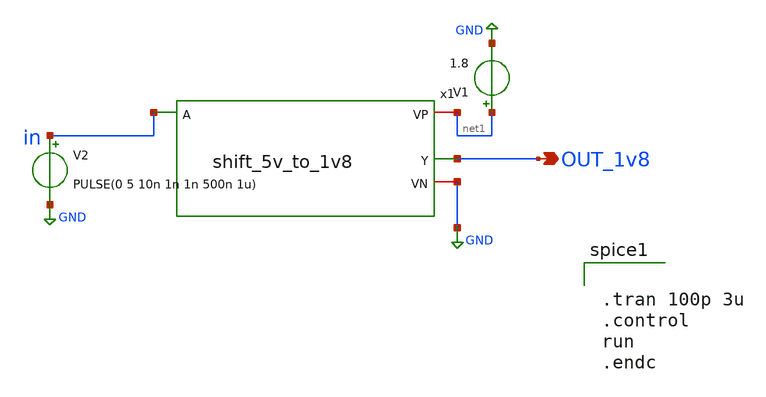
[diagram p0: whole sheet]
** sch_path: ADC/16bit_C2C/MagicAndSpice/shift_5v_to_1v8_TB.sch
**.subckt shift_5v_to_1v8_TB OUT_1v8
*.opin OUT_1v8
V1 net1 GND 1.8
V2 in GND PULSE(0 5 10n 1n 1n 500n 1u)
x1 net1 in OUT_1v8 GND shift_5v_to_1v8
**** begin user architecture code
 .lib $::SKYWATER_MODELS/sky130.lib.spice tt


.tran 100p 3u
.control
run
.endc

**** end user architecture code
**.ends
.GLOBAL GND
.end
